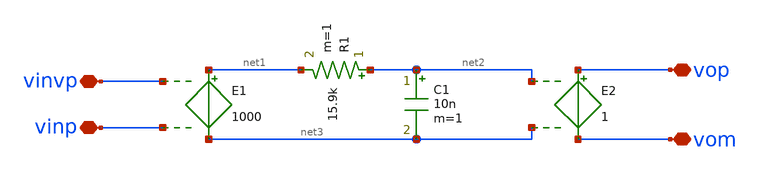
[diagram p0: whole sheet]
** sch_path: xschem/opam_hpf.sch
**.subckt opam_hpf vinp vinvp vop vom
*.iopin vinp
*.iopin vinvp
*.iopin vop
*.iopin vom
E1 net1 net3 vinvp vinp 1000
E2 vop vom net2 net3 1
C1 net2 net3 10n m=1
R1 net2 net1 15.9k m=1
**.ends
.end
